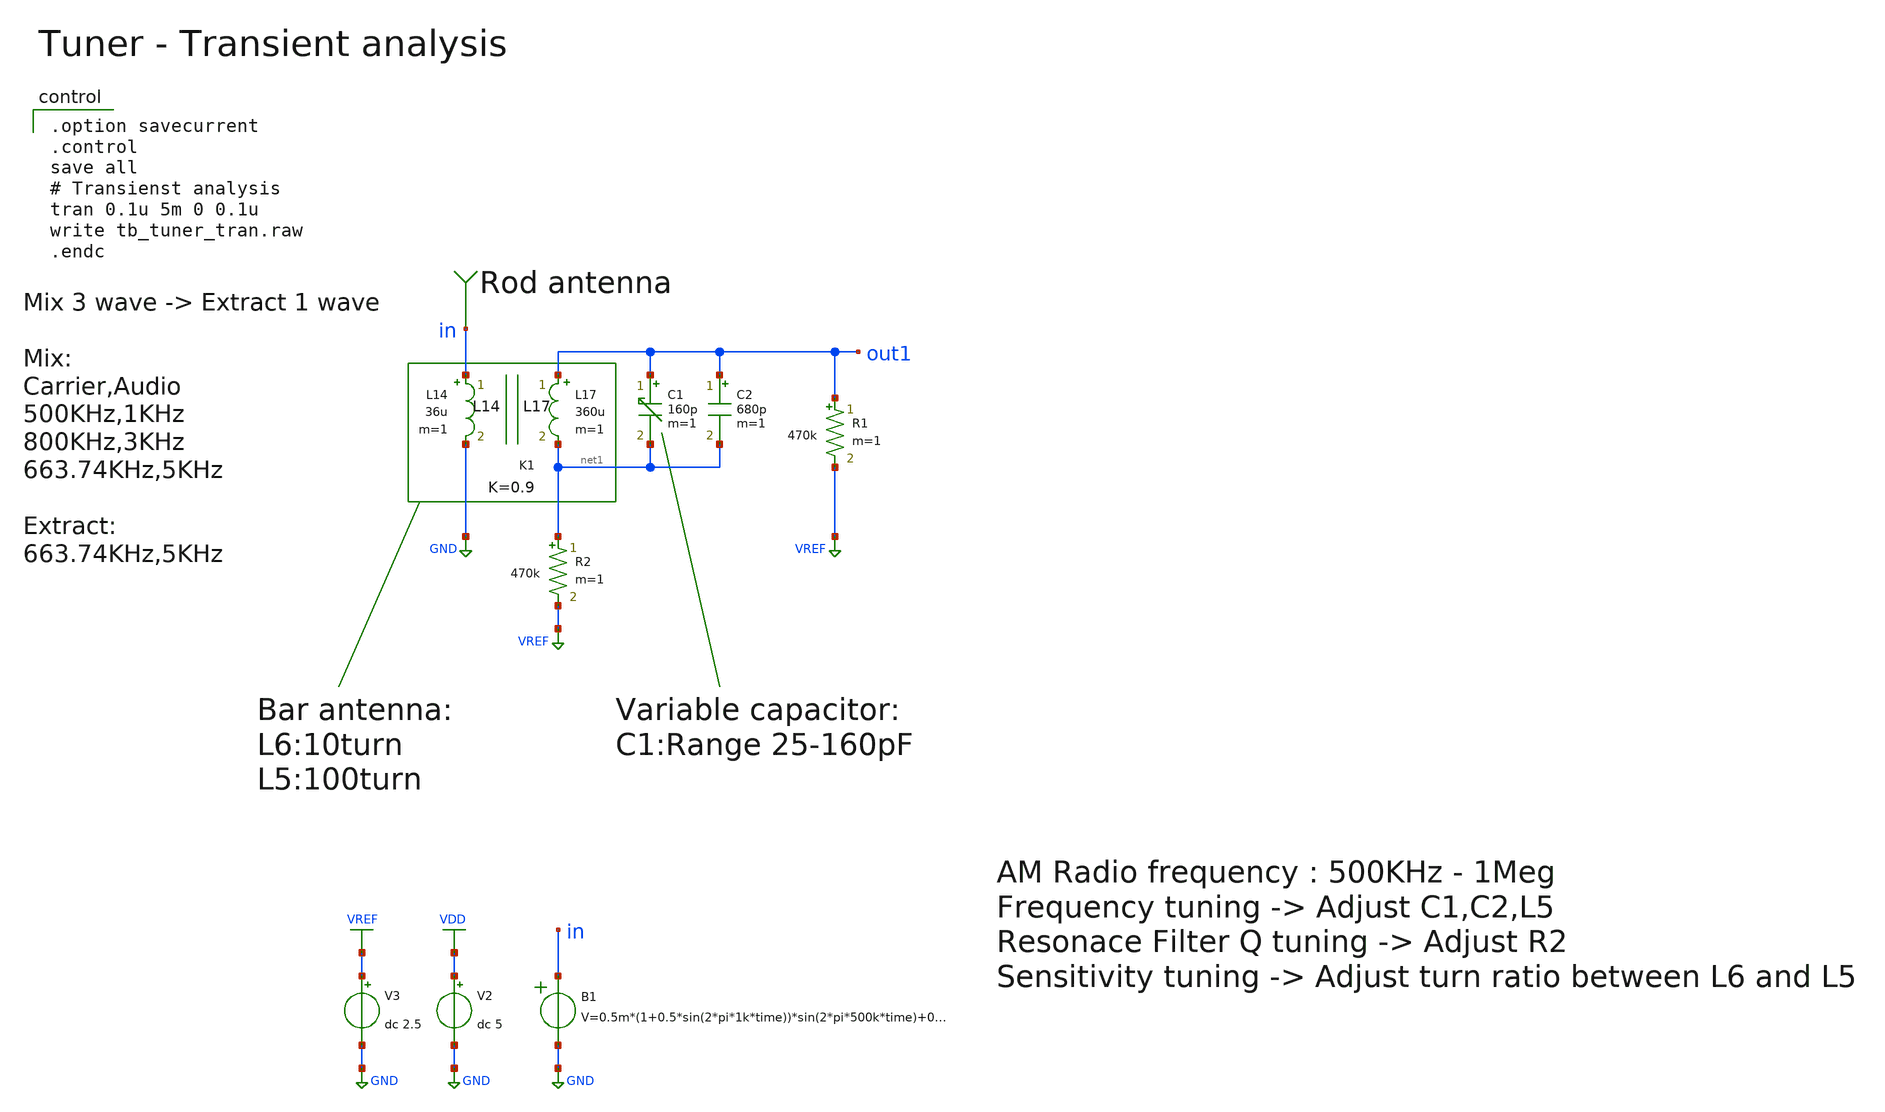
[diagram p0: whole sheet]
** sch_path: member_project/AM_Radio/Yamada3/xschem/tb_tuner_tran.sch
**.subckt tb_tuner_tran
V2 VDD GND dc 5
V3 VREF GND dc 2.5
B1 in GND
+ V=0.5m*(1+0.5*sin(2*pi*1k*time))*sin(2*pi*500k*time)+0.5m*(1+0.5*sin(2*pi*3k*time))*sin(2*pi*800k*time)+0.5m*(1+0.5*sin(2*pi*5k*time))*sin(2*pi*663.74k*time)
C1 out1 net1 160p m=1
L14 in GND 36u m=1
K1 L17 L14 0.9
L17 out1 net1 360u m=1
R1 out1 VREF 470k m=1
R2 net1 VREF 470k m=1
C2 out1 net1 680p m=1
**** begin user architecture code

.option savecurrent
.control
save all
# Transienst analysis
tran 0.1u 5m 0 0.1u
write tb_tuner_tran.raw
.endc

 .include $::LIB/ip62_models
**** end user architecture code
**.ends
.GLOBAL GND
.GLOBAL VDD
.GLOBAL VREF
.end
